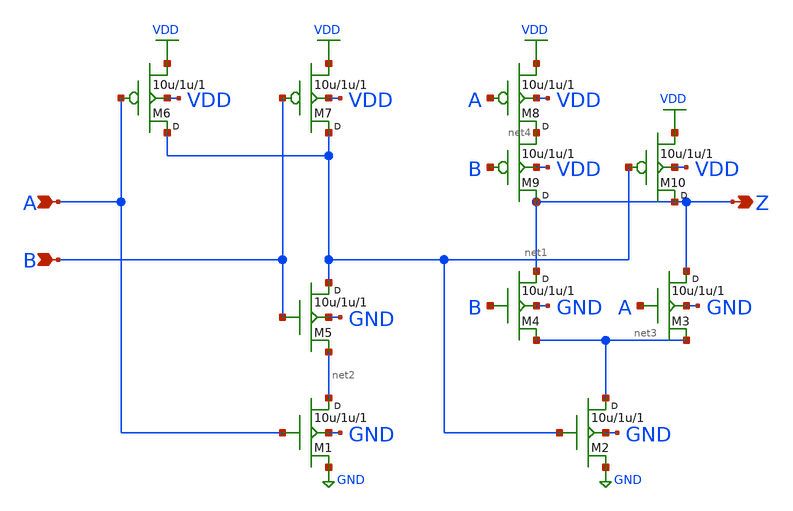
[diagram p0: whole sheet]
** sch_path: xschem_libraries_oa/examples/xnor/schematic/xnor.sch
* Copyright (C) 1998-2024 Stefan Frederik Schippers
* This program is free software; you can redistribute it and/or modify
* it under the terms of the GNU General Public License as published by
* the Free Software Foundation; either version 2 of the License, or
* (at your option) any later version.
* This program is distributed in the hope that it will be useful,
* but WITHOUT ANY WARRANTY; without even the implied warranty of
* MERCHANTABILITY or FITNESS FOR A PARTICULAR PURPOSE.  See the
* GNU General Public License for more details.
* You should have received a copy of the GNU General Public License
* along with this program; if not, write to the Free Software
**.subckt xnor B Z A
*.ipin B
*.opin Z
*.ipin A
M1 net2 A GND GND nmos w=10u l=1u m=1
M2 net3 net1 GND GND nmos w=10u l=1u m=1
M3 Z A net3 GND nmos w=10u l=1u m=1
M4 Z B net3 GND nmos w=10u l=1u m=1
M5 net1 B net2 GND nmos w=10u l=1u m=1
M6 net1 A VDD VDD pmos w=10u l=1u m=1
M7 net1 B VDD VDD pmos w=10u l=1u m=1
M8 net4 A VDD VDD pmos w=10u l=1u m=1
M9 Z B net4 VDD pmos w=10u l=1u m=1
M10 Z net1 VDD VDD pmos w=10u l=1u m=1
**.ends
.GLOBAL GND
.GLOBAL VDD
.end
